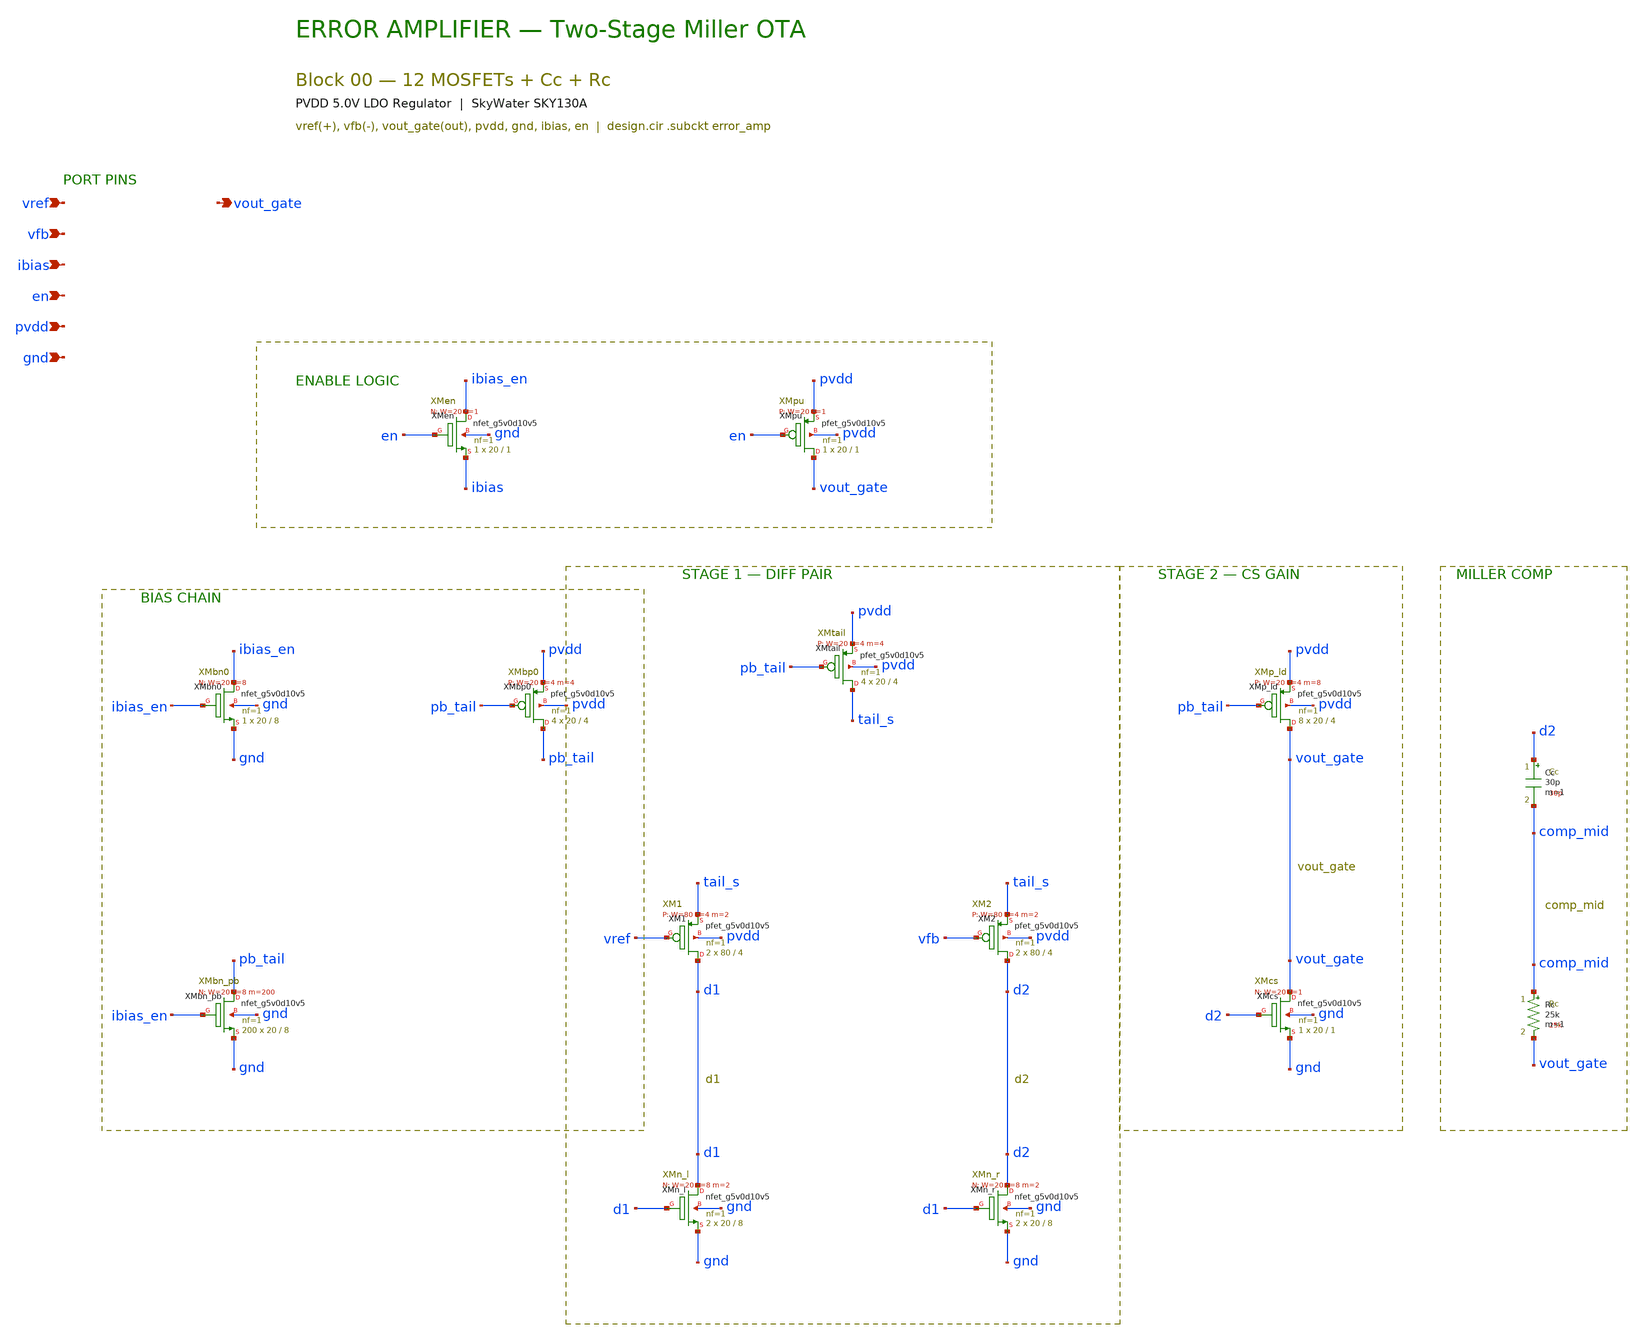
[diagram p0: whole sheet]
** sch_path: pvdd_regulator/10_top_integration/schematics/pvdd_00_error_amp.sch
**.subckt pvdd_00_error_amp vref vfb ibias en pvdd gnd vout_gate
*.ipin vref
*.ipin vfb
*.ipin ibias
*.ipin en
*.ipin pvdd
*.ipin gnd
*.opin vout_gate
XXMen ibias_en en ibias gnd sky130_fd_pr__nfet_g5v0d10v5 L=1 W=20 nf=1 ad='int((1 + 1)/2) * 20 / 1 * 0.29'
+ as='int((1 + 2)/2) * 20 / 1 * 0.29' pd='2*int((1 + 1)/2) * (20 / 1 + 0.29)' ps='2*int((1 + 2)/2) * (20 / 1 + 0.29)'
+ nrd='0.29 / 20 ' nrs='0.29 / 20 ' sa=0 sb=0 sd=0 mult=1 m=1
XXMpu vout_gate en pvdd pvdd sky130_fd_pr__pfet_g5v0d10v5 L=1 W=20 nf=1 ad='int((1 + 1)/2) * 20 / 1 * 0.29'
+ as='int((1 + 2)/2) * 20 / 1 * 0.29' pd='2*int((1 + 1)/2) * (20 / 1 + 0.29)' ps='2*int((1 + 2)/2) * (20 / 1 + 0.29)'
+ nrd='0.29 / 20 ' nrs='0.29 / 20 ' sa=0 sb=0 sd=0 mult=1 m=1
XXMbn0 ibias_en ibias_en gnd gnd sky130_fd_pr__nfet_g5v0d10v5 L=8 W=20 nf=1 ad='int((1 + 1)/2) * 20 / 1 * 0.29'
+ as='int((1 + 2)/2) * 20 / 1 * 0.29' pd='2*int((1 + 1)/2) * (20 / 1 + 0.29)' ps='2*int((1 + 2)/2) * (20 / 1 + 0.29)'
+ nrd='0.29 / 20 ' nrs='0.29 / 20 ' sa=0 sb=0 sd=0 mult=1 m=1
XXMbn_pb pb_tail ibias_en gnd gnd sky130_fd_pr__nfet_g5v0d10v5 L=8 W=20 nf=1 ad='int((1 + 1)/2) * 20 / 1 * 0.29'
+ as='int((1 + 2)/2) * 20 / 1 * 0.29' pd='2*int((1 + 1)/2) * (20 / 1 + 0.29)' ps='2*int((1 + 2)/2) * (20 / 1 + 0.29)'
+ nrd='0.29 / 20 ' nrs='0.29 / 20 ' sa=0 sb=0 sd=0 mult=200 m=200
XXMbp0 pb_tail pb_tail pvdd pvdd sky130_fd_pr__pfet_g5v0d10v5 L=4 W=20 nf=1 ad='int((1 + 1)/2) * 20 / 1 * 0.29'
+ as='int((1 + 2)/2) * 20 / 1 * 0.29' pd='2*int((1 + 1)/2) * (20 / 1 + 0.29)' ps='2*int((1 + 2)/2) * (20 / 1 + 0.29)'
+ nrd='0.29 / 20 ' nrs='0.29 / 20 ' sa=0 sb=0 sd=0 mult=4 m=4
XXMtail tail_s pb_tail pvdd pvdd sky130_fd_pr__pfet_g5v0d10v5 L=4 W=20 nf=1 ad='int((1 + 1)/2) * 20 / 1 * 0.29'
+ as='int((1 + 2)/2) * 20 / 1 * 0.29' pd='2*int((1 + 1)/2) * (20 / 1 + 0.29)' ps='2*int((1 + 2)/2) * (20 / 1 + 0.29)'
+ nrd='0.29 / 20 ' nrs='0.29 / 20 ' sa=0 sb=0 sd=0 mult=4 m=4
XXM1 d1 vref tail_s pvdd sky130_fd_pr__pfet_g5v0d10v5 L=4 W=80 nf=1 ad='int((1 + 1)/2) * 80 / 1 * 0.29'
+ as='int((1 + 2)/2) * 80 / 1 * 0.29' pd='2*int((1 + 1)/2) * (80 / 1 + 0.29)' ps='2*int((1 + 2)/2) * (80 / 1 + 0.29)'
+ nrd='0.29 / 80 ' nrs='0.29 / 80 ' sa=0 sb=0 sd=0 mult=2 m=2
XXM2 d2 vfb tail_s pvdd sky130_fd_pr__pfet_g5v0d10v5 L=4 W=80 nf=1 ad='int((1 + 1)/2) * 80 / 1 * 0.29'
+ as='int((1 + 2)/2) * 80 / 1 * 0.29' pd='2*int((1 + 1)/2) * (80 / 1 + 0.29)' ps='2*int((1 + 2)/2) * (80 / 1 + 0.29)'
+ nrd='0.29 / 80 ' nrs='0.29 / 80 ' sa=0 sb=0 sd=0 mult=2 m=2
XXMn_l d1 d1 gnd gnd sky130_fd_pr__nfet_g5v0d10v5 L=8 W=20 nf=1 ad='int((1 + 1)/2) * 20 / 1 * 0.29' as='int((1 + 2)/2) * 20 / 1 * 0.29'
+ pd='2*int((1 + 1)/2) * (20 / 1 + 0.29)' ps='2*int((1 + 2)/2) * (20 / 1 + 0.29)' nrd='0.29 / 20 ' nrs='0.29 / 20 '
+ sa=0 sb=0 sd=0 mult=2 m=2
XXMn_r d2 d1 gnd gnd sky130_fd_pr__nfet_g5v0d10v5 L=8 W=20 nf=1 ad='int((1 + 1)/2) * 20 / 1 * 0.29' as='int((1 + 2)/2) * 20 / 1 * 0.29'
+ pd='2*int((1 + 1)/2) * (20 / 1 + 0.29)' ps='2*int((1 + 2)/2) * (20 / 1 + 0.29)' nrd='0.29 / 20 ' nrs='0.29 / 20 '
+ sa=0 sb=0 sd=0 mult=2 m=2
XXMp_ld vout_gate pb_tail pvdd pvdd sky130_fd_pr__pfet_g5v0d10v5 L=4 W=20 nf=1 ad='int((1 + 1)/2) * 20 / 1 * 0.29'
+ as='int((1 + 2)/2) * 20 / 1 * 0.29' pd='2*int((1 + 1)/2) * (20 / 1 + 0.29)' ps='2*int((1 + 2)/2) * (20 / 1 + 0.29)'
+ nrd='0.29 / 20 ' nrs='0.29 / 20 ' sa=0 sb=0 sd=0 mult=8 m=8
XXMcs vout_gate d2 gnd gnd sky130_fd_pr__nfet_g5v0d10v5 L=1 W=20 nf=1 ad='int((1 + 1)/2) * 20 / 1 * 0.29'
+ as='int((1 + 2)/2) * 20 / 1 * 0.29' pd='2*int((1 + 1)/2) * (20 / 1 + 0.29)' ps='2*int((1 + 2)/2) * (20 / 1 + 0.29)'
+ nrd='0.29 / 20 ' nrs='0.29 / 20 ' sa=0 sb=0 sd=0 mult=1 m=1
Cc d2 comp_mid 30p m=1
Rc comp_mid vout_gate 25k m=1
**.ends
.end
